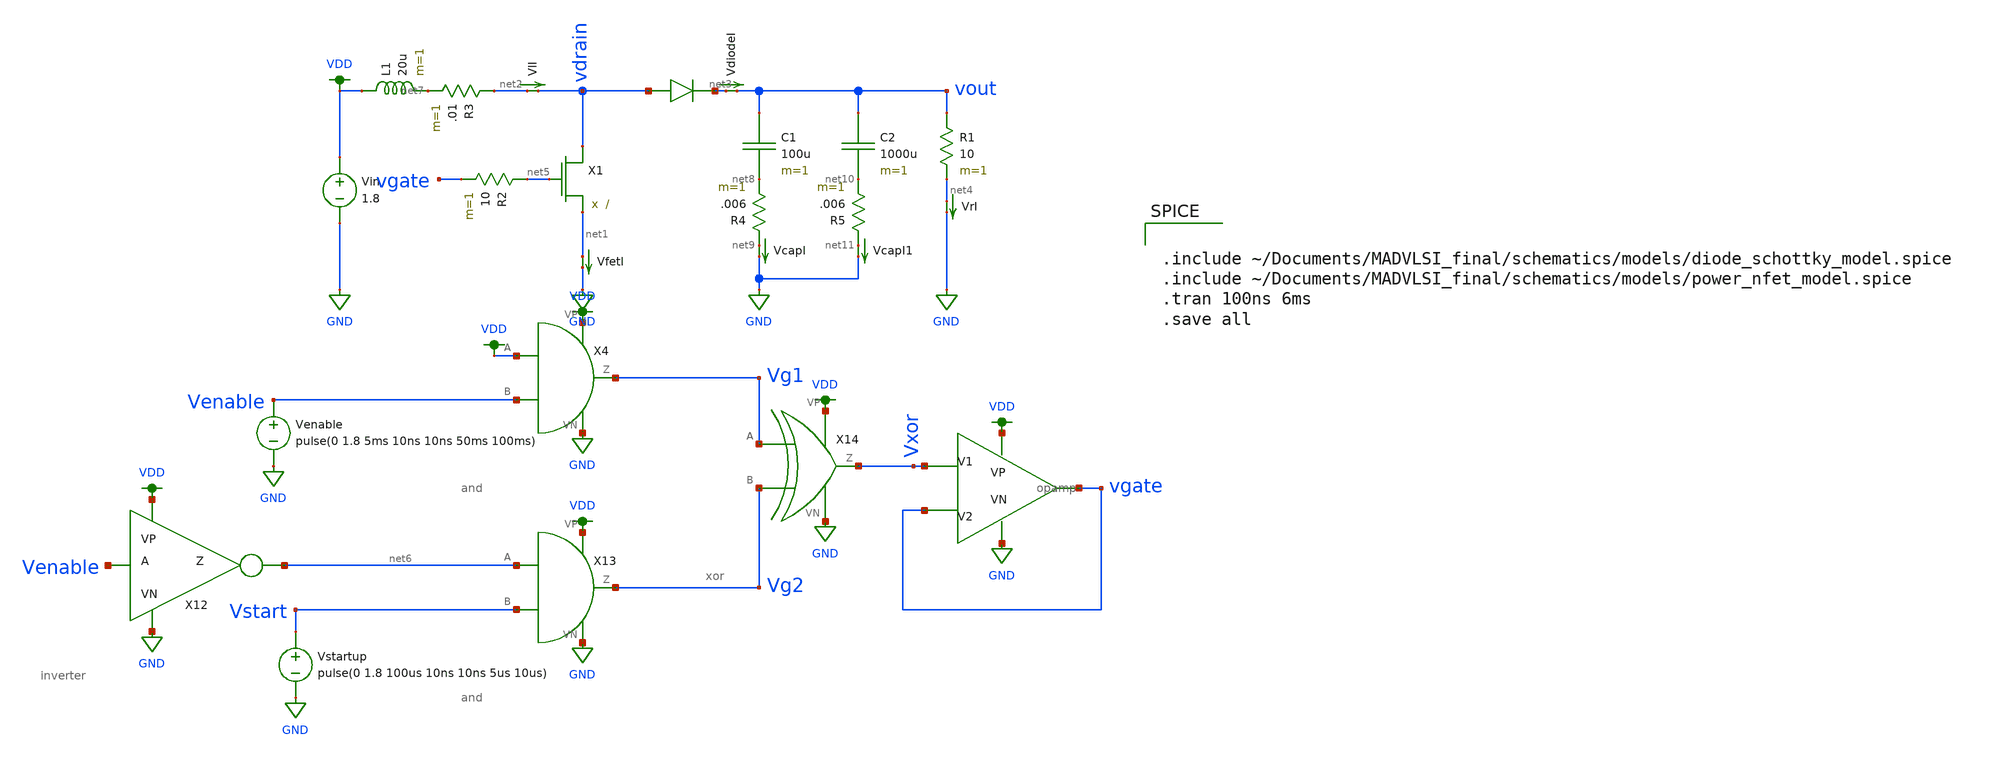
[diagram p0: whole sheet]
** sch_path: schematics/old/simple_boost_circuit.sch
**.subckt simple_boost_circuit
Vin VDD GND 1.8
VfetI net1 GND 0
.save i(vfeti)
X1 vdrain net5 net1 power_nfet
L1 VDD net7 20u m=1
D1 vdrain net3 diode_schottky
C1 vout net8 100u m=1
R1 vout net4 10 m=1
VlI net2 vdrain 0
.save i(vli)
VcapI net9 GND 0
.save i(vcapi)
VrI net4 GND 0
.save i(vri)
R2 net5 vgate 10 m=1
R3 net2 net7 .01 m=1
R4 net9 net8 .006 m=1
VdiodeI net3 vout 0
.save i(vdiodei)
X4 VDD Venable VDD GND Vg1 and
X12 Venable VDD GND net6 inverter
Venable Venable GND pulse(0 1.8 5ms 10ns 10ns 50ms 100ms)
X13 net6 Vstart VDD GND Vg2 and
Vstartup Vstart GND pulse(0 1.8 100us 10ns 10ns 5us 10us)
X14 Vg1 Vg2 VDD GND Vxor xor
X15 Vxor vgate VDD GND vgate opamp
C2 vout net10 1000u m=1
VcapI1 net11 GND 0
.save i(vcapi1)
R5 net11 net10 .006 m=1
**** begin user architecture code


.include ~/Documents/MADVLSI_final/schematics/models/diode_schottky_model.spice
.include ~/Documents/MADVLSI_final/schematics/models/power_nfet_model.spice
.tran 100ns 6ms
.save all


.option wnflag=1
.lib ~/skywater/skywater-pdk/libraries/sky130_fd_pr_ngspice/latest/models/sky130.lib.spice tt

**** end user architecture code
**.ends

* expanding   symbol:  /home/madvlsi/Documents/MADVLSI_final/schematics/and.sym # of pins=6
** sym_path: schematics/and.sym
** sch_path: schematics/and.sch
.subckt and A B VP VN Z
*.ipin A
*.ipin B
*.iopin VP
*.iopin VN
*.opin Z
X1 net1 VP VN Z inverter
X2 A B VP VN net1 nand
**** begin user architecture code

.param l=.15
.param w=1
.param mn=1
.param mp=1

**** end user architecture code
.ends


* expanding   symbol:  /home/madvlsi/Documents/MADVLSI_final/schematics/inverter.sym # of pins=4
** sym_path: schematics/inverter.sym
** sch_path: schematics/inverter.sch
.subckt inverter A VP VN Z
*.ipin A
*.iopin VP
*.iopin VN
*.opin Z
XM1 Z A VN GND sky130_fd_pr__nfet_01v8 L=0.15 W=1 nf=1 ad='int((nf+1)/2) * W/nf * 0.29' as='int((nf+2)/2) * W/nf * 0.29'
+ pd='2*int((nf+1)/2) * (W/nf + 0.29)' ps='2*int((nf+2)/2) * (W/nf + 0.29)' nrd='0.29 / W' nrs='0.29 / W'
+ sa=0 sb=0 sd=0 mult=1 m=1
XM2 Z A VP VDD sky130_fd_pr__pfet_01v8 L=0.15 W=1 nf=1 ad='int((nf+1)/2) * W/nf * 0.29' as='int((nf+2)/2) * W/nf * 0.29'
+ pd='2*int((nf+1)/2) * (W/nf + 0.29)' ps='2*int((nf+2)/2) * (W/nf + 0.29)' nrd='0.29 / W' nrs='0.29 / W'
+ sa=0 sb=0 sd=0 mult=2 m=2
**** begin user architecture code

.param l=.15
.param w=1
.param mn=1
.param mp=1

**** end user architecture code
.ends


* expanding   symbol:  /home/madvlsi/Documents/MADVLSI_final/schematics/xor.sym # of pins=6
** sym_path: schematics/xor.sym
** sch_path: schematics/xor.sch
.subckt xor A B VP VN Z
*.ipin A
*.ipin B
*.iopin VP
*.iopin VN
*.opin Z
X1 A B VP VN net1 nand
X2 net1 B VP VN net2 nand
X3 A net1 VP VN net3 nand
X4 net3 net2 VP VN Z nand
**** begin user architecture code

.param l=.15
.param w=1
.param mn=1
.param mp=1

**** end user architecture code
.ends


* expanding   symbol:  /home/madvlsi/Documents/MADVLSI_final/schematics/opamp.sym # of pins=5
** sym_path: schematics/opamp.sym
** sch_path: schematics/opamp.sch
.subckt opamp V1 V2 VP VN Vout
*.ipin V1
*.ipin V2
*.opin Vout
*.iopin VP
*.iopin VN
*.iopin VP
*.iopin VN
XM1 VN net7 net2 GND sky130_fd_pr__nfet_01v8 L=l W=w nf=1 ad='int((nf+1)/2) * W/nf * 0.29' as='int((nf+2)/2) * W/nf * 0.29'
+ pd='2*int((nf+1)/2) * (W/nf + 0.29)' ps='2*int((nf+2)/2) * (W/nf + 0.29)' nrd='0.29 / W' nrs='0.29 / W'
+ sa=0 sb=0 sd=0 mult=1 m=1
XM2 VP net3 net1 VDD sky130_fd_pr__pfet_01v8 L=l W=w nf=1 ad='int((nf+1)/2) * W/nf * 0.29' as='int((nf+2)/2) * W/nf * 0.29'
+ pd='2*int((nf+1)/2) * (W/nf + 0.29)' ps='2*int((nf+2)/2) * (W/nf + 0.29)' nrd='0.29 / W' nrs='0.29 / W'
+ sa=0 sb=0 sd=0 mult=1 m=1
XM3 net1 V1 Vd VDD sky130_fd_pr__pfet_01v8 L=l W=w nf=1 ad='int((nf+1)/2) * W/nf * 0.29' as='int((nf+2)/2) * W/nf * 0.29'
+ pd='2*int((nf+1)/2) * (W/nf + 0.29)' ps='2*int((nf+2)/2) * (W/nf + 0.29)' nrd='0.29 / W' nrs='0.29 / W'
+ sa=0 sb=0 sd=0 mult=1 m=1
XM4 Vc V2 net1 VDD sky130_fd_pr__pfet_01v8 L=l W=w nf=1 ad='int((nf+1)/2) * W/nf * 0.29' as='int((nf+2)/2) * W/nf * 0.29'
+ pd='2*int((nf+1)/2) * (W/nf + 0.29)' ps='2*int((nf+2)/2) * (W/nf + 0.29)' nrd='0.29 / W' nrs='0.29 / W'
+ sa=0 sb=0 sd=0 mult=1 m=1
XM5 Va V2 net2 GND sky130_fd_pr__nfet_01v8 L=l W=w nf=1 ad='int((nf+1)/2) * W/nf * 0.29' as='int((nf+2)/2) * W/nf * 0.29'
+ pd='2*int((nf+1)/2) * (W/nf + 0.29)' ps='2*int((nf+2)/2) * (W/nf + 0.29)' nrd='0.29 / W' nrs='0.29 / W'
+ sa=0 sb=0 sd=0 mult=1 m=1
XM6 net2 V1 Vb GND sky130_fd_pr__nfet_01v8 L=l W=w nf=1 ad='int((nf+1)/2) * W/nf * 0.29' as='int((nf+2)/2) * W/nf * 0.29'
+ pd='2*int((nf+1)/2) * (W/nf + 0.29)' ps='2*int((nf+2)/2) * (W/nf + 0.29)' nrd='0.29 / W' nrs='0.29 / W'
+ sa=0 sb=0 sd=0 mult=1 m=1
XM7 net3 net3 Va VDD sky130_fd_pr__pfet_01v8 L=l W=w nf=1 ad='int((nf+1)/2) * W/nf * 0.29' as='int((nf+2)/2) * W/nf * 0.29'
+ pd='2*int((nf+1)/2) * (W/nf + 0.29)' ps='2*int((nf+2)/2) * (W/nf + 0.29)' nrd='0.29 / W' nrs='0.29 / W'
+ sa=0 sb=0 sd=0 mult=1 m=1
XM8 net6 net6 Va VDD sky130_fd_pr__pfet_01v8 L=l W=w nf=1 ad='int((nf+1)/2) * W/nf * 0.29' as='int((nf+2)/2) * W/nf * 0.29'
+ pd='2*int((nf+1)/2) * (W/nf + 0.29)' ps='2*int((nf+2)/2) * (W/nf + 0.29)' nrd='0.29 / W' nrs='0.29 / W'
+ sa=0 sb=0 sd=0 mult=1 m=1
XM9 net5 net6 Vb VDD sky130_fd_pr__pfet_01v8 L=l W=w nf=1 ad='int((nf+1)/2) * W/nf * 0.29' as='int((nf+2)/2) * W/nf * 0.29'
+ pd='2*int((nf+1)/2) * (W/nf + 0.29)' ps='2*int((nf+2)/2) * (W/nf + 0.29)' nrd='0.29 / W' nrs='0.29 / W'
+ sa=0 sb=0 sd=0 mult=1 m=1
XM10 Va net3 VP VDD sky130_fd_pr__pfet_01v8 L=l W=w nf=1 ad='int((nf+1)/2) * W/nf * 0.29' as='int((nf+2)/2) * W/nf * 0.29'
+ pd='2*int((nf+1)/2) * (W/nf + 0.29)' ps='2*int((nf+2)/2) * (W/nf + 0.29)' nrd='0.29 / W' nrs='0.29 / W'
+ sa=0 sb=0 sd=0 mult=1 m=1
XM11 Vb net3 VP VDD sky130_fd_pr__pfet_01v8 L=l W=w nf=1 ad='int((nf+1)/2) * W/nf * 0.29' as='int((nf+2)/2) * W/nf * 0.29'
+ pd='2*int((nf+1)/2) * (W/nf + 0.29)' ps='2*int((nf+2)/2) * (W/nf + 0.29)' nrd='0.29 / W' nrs='0.29 / W'
+ sa=0 sb=0 sd=0 mult=1 m=1
XM12 net6 net6 Vc GND sky130_fd_pr__nfet_01v8 L=l W=w nf=1 ad='int((nf+1)/2) * W/nf * 0.29' as='int((nf+2)/2) * W/nf * 0.29'
+ pd='2*int((nf+1)/2) * (W/nf + 0.29)' ps='2*int((nf+2)/2) * (W/nf + 0.29)' nrd='0.29 / W' nrs='0.29 / W'
+ sa=0 sb=0 sd=0 mult=1 m=1
XM13 net5 net6 Vd GND sky130_fd_pr__nfet_01v8 L=l W=w nf=1 ad='int((nf+1)/2) * W/nf * 0.29' as='int((nf+2)/2) * W/nf * 0.29'
+ pd='2*int((nf+1)/2) * (W/nf + 0.29)' ps='2*int((nf+2)/2) * (W/nf + 0.29)' nrd='0.29 / W' nrs='0.29 / W'
+ sa=0 sb=0 sd=0 mult=1 m=1
XM14 Vc net7 VN GND sky130_fd_pr__nfet_01v8 L=l W=w nf=1 ad='int((nf+1)/2) * W/nf * 0.29' as='int((nf+2)/2) * W/nf * 0.29'
+ pd='2*int((nf+1)/2) * (W/nf + 0.29)' ps='2*int((nf+2)/2) * (W/nf + 0.29)' nrd='0.29 / W' nrs='0.29 / W'
+ sa=0 sb=0 sd=0 mult=1 m=1
XM15 Vd net7 VN GND sky130_fd_pr__nfet_01v8 L=l W=w nf=1 ad='int((nf+1)/2) * W/nf * 0.29' as='int((nf+2)/2) * W/nf * 0.29'
+ pd='2*int((nf+1)/2) * (W/nf + 0.29)' ps='2*int((nf+2)/2) * (W/nf + 0.29)' nrd='0.29 / W' nrs='0.29 / W'
+ sa=0 sb=0 sd=0 mult=1 m=1
XM16 net8 net7 net3 GND sky130_fd_pr__nfet_01v8 L=l W=w nf=1 ad='int((nf+1)/2) * W/nf * 0.29' as='int((nf+2)/2) * W/nf * 0.29'
+ pd='2*int((nf+1)/2) * (W/nf + 0.29)' ps='2*int((nf+2)/2) * (W/nf + 0.29)' nrd='0.29 / W' nrs='0.29 / W'
+ sa=0 sb=0 sd=0 mult=1 m=1
XM17 VN net7 net8 GND sky130_fd_pr__nfet_01v8 L=l W=w nf=1 ad='int((nf+1)/2) * W/nf * 0.29' as='int((nf+2)/2) * W/nf * 0.29'
+ pd='2*int((nf+1)/2) * (W/nf + 0.29)' ps='2*int((nf+2)/2) * (W/nf + 0.29)' nrd='0.29 / W' nrs='0.29 / W'
+ sa=0 sb=0 sd=0 mult=1 m=1
XM18 net8 net7 VP GND sky130_fd_pr__nfet_01v8 L=l W=w nf=1 ad='int((nf+1)/2) * W/nf * 0.29' as='int((nf+2)/2) * W/nf * 0.29'
+ pd='2*int((nf+1)/2) * (W/nf + 0.29)' ps='2*int((nf+2)/2) * (W/nf + 0.29)' nrd='0.29 / W' nrs='0.29 / W'
+ sa=0 sb=0 sd=0 mult=M m=M
XM19 net4 net3 net7 VDD sky130_fd_pr__pfet_01v8 L=l W=w nf=1 ad='int((nf+1)/2) * W/nf * 0.29' as='int((nf+2)/2) * W/nf * 0.29'
+ pd='2*int((nf+1)/2) * (W/nf + 0.29)' ps='2*int((nf+2)/2) * (W/nf + 0.29)' nrd='0.29 / W' nrs='0.29 / W'
+ sa=0 sb=0 sd=0 mult=1 m=1
XM20 VP net3 net4 VDD sky130_fd_pr__pfet_01v8 L=l W=w nf=1 ad='int((nf+1)/2) * W/nf * 0.29' as='int((nf+2)/2) * W/nf * 0.29'
+ pd='2*int((nf+1)/2) * (W/nf + 0.29)' ps='2*int((nf+2)/2) * (W/nf + 0.29)' nrd='0.29 / W' nrs='0.29 / W'
+ sa=0 sb=0 sd=0 mult=1 m=1
XM21 net4 net3 VN VDD sky130_fd_pr__pfet_01v8 L=l W=w nf=1 ad='int((nf+1)/2) * W/nf * 0.29' as='int((nf+2)/2) * W/nf * 0.29'
+ pd='2*int((nf+1)/2) * (W/nf + 0.29)' ps='2*int((nf+2)/2) * (W/nf + 0.29)' nrd='0.29 / W' nrs='0.29 / W'
+ sa=0 sb=0 sd=0 mult=M m=M
XM22 net7 net7 Vc GND sky130_fd_pr__nfet_01v8 L=l W=w nf=1 ad='int((nf+1)/2) * W/nf * 0.29' as='int((nf+2)/2) * W/nf * 0.29'
+ pd='2*int((nf+1)/2) * (W/nf + 0.29)' ps='2*int((nf+2)/2) * (W/nf + 0.29)' nrd='0.29 / W' nrs='0.29 / W'
+ sa=0 sb=0 sd=0 mult=1 m=1
**** begin user architecture code

.param M=3
.param w=3
.param l=0.6


**** end user architecture code
XM23 Vout net5 VN GND sky130_fd_pr__nfet_01v8 L=.15 W=6 nf=1 ad='int((nf+1)/2) * W/nf * 0.29' as='int((nf+2)/2) * W/nf * 0.29'
+ pd='2*int((nf+1)/2) * (W/nf + 0.29)' ps='2*int((nf+2)/2) * (W/nf + 0.29)' nrd='0.29 / W' nrs='0.29 / W'
+ sa=0 sb=0 sd=0 mult=1 m=1
XM24 Vout net5 VP VDD sky130_fd_pr__pfet_01v8 L=.15 W=12 nf=1 ad='int((nf+1)/2) * W/nf * 0.29' as='int((nf+2)/2) * W/nf * 0.29'
+ pd='2*int((nf+1)/2) * (W/nf + 0.29)' ps='2*int((nf+2)/2) * (W/nf + 0.29)' nrd='0.29 / W' nrs='0.29 / W'
+ sa=0 sb=0 sd=0 mult=1 m=1
C1 Vout net5 500f m=1
.ends


* expanding   symbol:  /home/madvlsi/Documents/final/xschem/nand.sym # of pins=6
** sym_path: schematics/nand.sym
** sch_path: schematics/nand.sch
.subckt nand A B VP VN Z
*.ipin A
*.iopin VP
*.iopin VN
*.opin Z
*.ipin B
XM1 Z A net1 GND sky130_fd_pr__nfet_01v8 L=0.15 W=1 nf=1 ad='int((nf+1)/2) * W/nf * 0.29' as='int((nf+2)/2) * W/nf * 0.29'
+ pd='2*int((nf+1)/2) * (W/nf + 0.29)' ps='2*int((nf+2)/2) * (W/nf + 0.29)' nrd='0.29 / W' nrs='0.29 / W'
+ sa=0 sb=0 sd=0 mult=1 m=1
XM2 VP B Z VDD sky130_fd_pr__pfet_01v8 L=0.15 W=1 nf=1 ad='int((nf+1)/2) * W/nf * 0.29' as='int((nf+2)/2) * W/nf * 0.29'
+ pd='2*int((nf+1)/2) * (W/nf + 0.29)' ps='2*int((nf+2)/2) * (W/nf + 0.29)' nrd='0.29 / W' nrs='0.29 / W'
+ sa=0 sb=0 sd=0 mult=2 m=2
XM3 VN B net1 GND sky130_fd_pr__nfet_01v8 L=0.15 W=1 nf=1 ad='int((nf+1)/2) * W/nf * 0.29' as='int((nf+2)/2) * W/nf * 0.29'
+ pd='2*int((nf+1)/2) * (W/nf + 0.29)' ps='2*int((nf+2)/2) * (W/nf + 0.29)' nrd='0.29 / W' nrs='0.29 / W'
+ sa=0 sb=0 sd=0 mult=1 m=1
XM4 Z A VP VDD sky130_fd_pr__pfet_01v8 L=0.15 W=1 nf=1 ad='int((nf+1)/2) * W/nf * 0.29' as='int((nf+2)/2) * W/nf * 0.29'
+ pd='2*int((nf+1)/2) * (W/nf + 0.29)' ps='2*int((nf+2)/2) * (W/nf + 0.29)' nrd='0.29 / W' nrs='0.29 / W'
+ sa=0 sb=0 sd=0 mult=2 m=2
.ends

.GLOBAL GND
.GLOBAL VDD
.end
